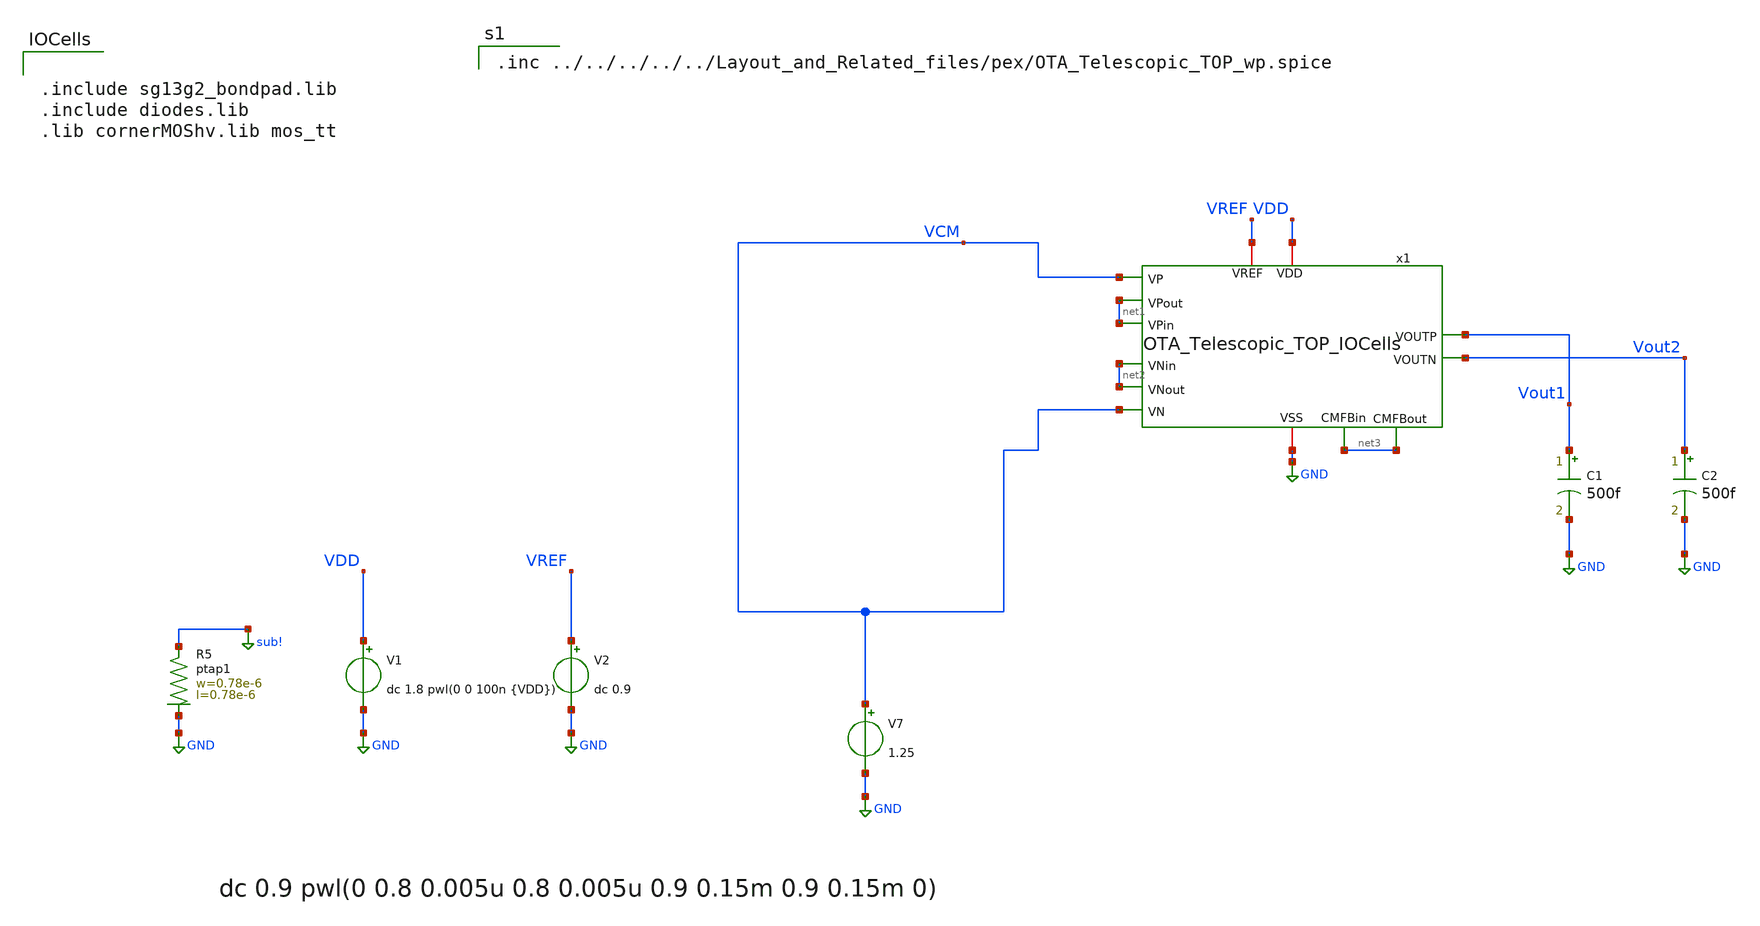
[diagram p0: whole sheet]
** sch_path: OTA_Telescopic/AutoTestbench/tb/done/OTA_Telescopic_TOP_TB_StartUp100n_io.sch
**.subckt OTA_Telescopic_TOP_TB_StartUp100n_io
V7 VCM GND 1.25
V1 VDD GND dc 1.8 pwl(0 0 100n {VDD})
V2 VREF GND dc 0.9
C1 Vout1 GND 500f m=1
C2 Vout2 GND 500f m=1
XR5 sub! GND ptap1 R=262.8 w=0.78e-6 l=0.78e-6
x1 VDD GND net1 VCM net1 Vout2 Vout1 net2 net2 VCM VREF net3 net3 OTA_Telescopic_TOP_IOCells
**** begin user architecture code


** opencircuitdesign pdks install
.lib cornerMOSlv.lib mos_$PROCESS
.lib cornerRES.lib res_typ
.lib cornerCAP.lib cap_typ
.temp $TEMP




.include sg13g2_bondpad.lib
.include diodes.lib
.lib cornerMOShv.lib mos_tt




.param VDD=$VDD
.control
save v(VDD) v(Vout1) v(Vout2) i(V1)
tran 10n 500n
*write NMOS_diode_large_signal.raw

let VCM = v(Vout1)
let VDD = v(VDD)
let IDD = -i(V1)

wrdata VCM_100ns_DC_io.txt VCM
wrdata IDD_100ns_DC_io.txt IDD
wrdata VDD_100ns_DC_io.txt VDD

plot VCM
plot VDD
plot IDD


let Vo = Vout1-Vout2

wrdata Vo Vo

.endc



.inc ../../../../../Layout_and_Related_files/pex/OTA_Telescopic_TOP_wp.spice

**** end user architecture code
**.ends
.GLOBAL GND
.GLOBAL sub!
.end
